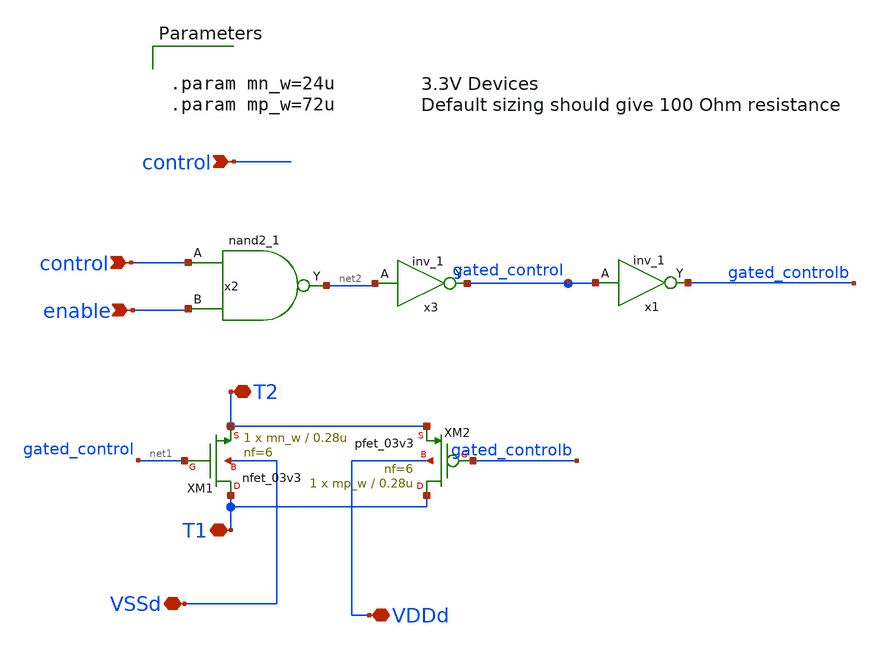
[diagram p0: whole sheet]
** sch_path: designs/switch_matrix_gf180mcu_9t5v0-main/swmatrix_Tgate/swmatrix_Tgate_PK.sch
**.subckt swmatrix_Tgate_PK T1 T2 control VDDd VSSd control enable
*.iopin T1
*.iopin T2
*.ipin control
*.iopin VDDd
*.iopin VSSd
*.ipin control
*.ipin enable
XM1 T1 net1 T2 VSSd nfet_03v3 L=0.28u W=mn_w nf=6 ad='int((nf+1)/2) * W/nf * 0.18u' as='int((nf+2)/2) * W/nf * 0.18u'
+ pd='2*int((nf+1)/2) * (W/nf + 0.18u)' ps='2*int((nf+2)/2) * (W/nf + 0.18u)' nrd='0.18u / W' nrs='0.18u / W'
+ sa=0 sb=0 sd=0 m=1
XM2 T1 gated_controlb T2 VDDd pfet_03v3 L=0.28u W=mp_w nf=6 ad='int((nf+1)/2) * W/nf * 0.18u' as='int((nf+2)/2) * W/nf * 0.18u'
+ pd='2*int((nf+1)/2) * (W/nf + 0.18u)' ps='2*int((nf+2)/2) * (W/nf + 0.18u)' nrd='0.18u / W' nrs='0.18u / W'
+ sa=0 sb=0 sd=0 m=1
x1 gated_control VSSd VDDd VSSd VDDd gated_controlb gf180mcu_fd_sc_mcu9t5v0__inv_1
x2 control enable VSSd VDDd VSSd VDDd net2 gf180mcu_fd_sc_mcu9t5v0__nand2_1
x3 net2 VSSd VDDd VSSd VDDd gated_control gf180mcu_fd_sc_mcu9t5v0__inv_1
**** begin user architecture code


.param mn_w=24u
.param mp_w=72u

**** end user architecture code
**.ends
.end
